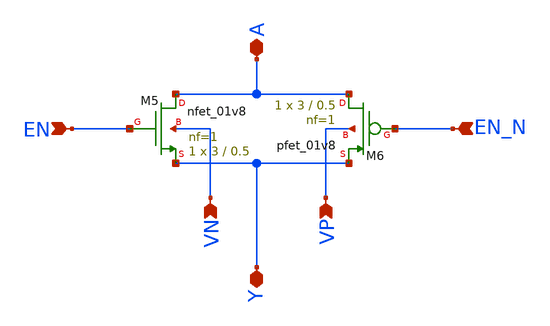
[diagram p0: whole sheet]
** sch_path: ADC/16bit_C2C/MagicAndSpice/EE431_FinalProj/TGATE.sch
**.subckt TGATE A Y EN EN_N VP VN
*.iopin A
*.iopin Y
*.ipin EN
*.ipin EN_N
*.ipin VP
*.ipin VN
XM5 A EN Y VN sky130_fd_pr__nfet_01v8 L=0.5 W=3 nf=1 ad='int((nf+1)/2) * W/nf * 0.29' as='int((nf+2)/2) * W/nf * 0.29'
+ pd='2*int((nf+1)/2) * (W/nf + 0.29)' ps='2*int((nf+2)/2) * (W/nf + 0.29)' nrd='0.29 / W' nrs='0.29 / W'
+ sa=0 sb=0 sd=0 mult=1 m=1
XM6 A EN_N Y VP sky130_fd_pr__pfet_01v8 L=0.5 W=3 nf=1 ad='int((nf+1)/2) * W/nf * 0.29' as='int((nf+2)/2) * W/nf * 0.29'
+ pd='2*int((nf+1)/2) * (W/nf + 0.29)' ps='2*int((nf+2)/2) * (W/nf + 0.29)' nrd='0.29 / W' nrs='0.29 / W'
+ sa=0 sb=0 sd=0 mult=1 m=1
**** begin user architecture code
type=subcircuit
**** end user architecture code
**.ends
.end
